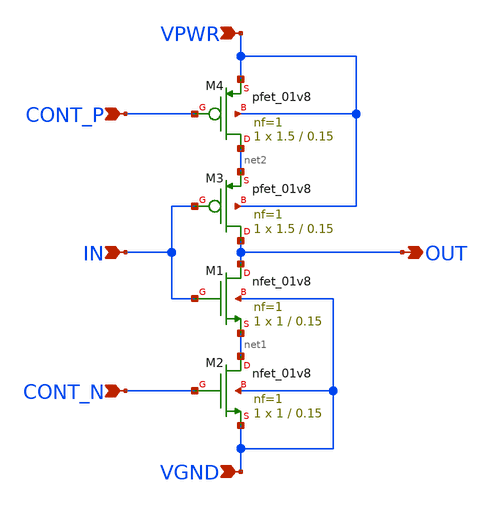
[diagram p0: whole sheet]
** sch_path: xschem/ring_osc/delay_cell.sch
**.subckt delay_cell VPWR VGND IN CONT_N CONT_P OUT
*.ipin VPWR
*.ipin VGND
*.ipin IN
*.ipin CONT_N
*.ipin CONT_P
*.opin OUT
XM1 OUT IN net1 VGND sky130_fd_pr__nfet_01v8 L=0.15 W=1 nf=1 ad='int((nf+1)/2) * W/nf * 0.29' as='int((nf+2)/2) * W/nf * 0.29'
+ pd='2*int((nf+1)/2) * (W/nf + 0.29)' ps='2*int((nf+2)/2) * (W/nf + 0.29)' nrd='0.29 / W' nrs='0.29 / W'
+ sa=0 sb=0 sd=0 mult=1 m=1
XM2 net1 CONT_N VGND VGND sky130_fd_pr__nfet_01v8 L=0.15 W=1 nf=1 ad='int((nf+1)/2) * W/nf * 0.29' as='int((nf+2)/2) * W/nf * 0.29'
+ pd='2*int((nf+1)/2) * (W/nf + 0.29)' ps='2*int((nf+2)/2) * (W/nf + 0.29)' nrd='0.29 / W' nrs='0.29 / W'
+ sa=0 sb=0 sd=0 mult=1 m=1
XM3 OUT IN net2 VPWR sky130_fd_pr__pfet_01v8 L=0.15 W=1.5 nf=1 ad='int((nf+1)/2) * W/nf * 0.29' as='int((nf+2)/2) * W/nf * 0.29'
+ pd='2*int((nf+1)/2) * (W/nf + 0.29)' ps='2*int((nf+2)/2) * (W/nf + 0.29)' nrd='0.29 / W' nrs='0.29 / W'
+ sa=0 sb=0 sd=0 mult=1 m=1
XM4 net2 CONT_P VPWR VPWR sky130_fd_pr__pfet_01v8 L=0.15 W=1.5 nf=1 ad='int((nf+1)/2) * W/nf * 0.29'
+ as='int((nf+2)/2) * W/nf * 0.29' pd='2*int((nf+1)/2) * (W/nf + 0.29)' ps='2*int((nf+2)/2) * (W/nf + 0.29)'
+ nrd='0.29 / W' nrs='0.29 / W' sa=0 sb=0 sd=0 mult=1 m=1
**.ends
.end
